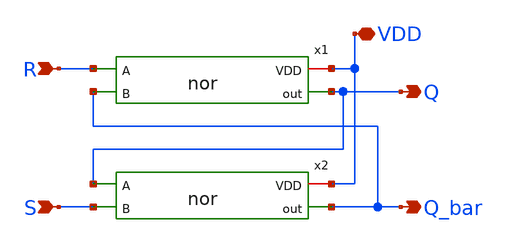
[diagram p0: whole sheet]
** sch_path: xschem/RS_latch.sch
**.subckt RS_latch VDD Q Q_bar R S
*.iopin VDD
*.opin Q
*.opin Q_bar
*.ipin R
*.ipin S
x1 VDD R Q_bar Q nor
x2 VDD Q S Q_bar nor
**.ends

* expanding   symbol:  nor.sym # of pins=4
** sym_path: xschem/nor.sym
** sch_path: xschem/nor.sch
.subckt nor VDD A B out
*.iopin VDD
*.ipin A
*.ipin B
*.opin out
XM1 out B GND GND sky130_fd_pr__nfet_01v8 L=0.18 W=0.42 nf=1 ad='int((nf+1)/2) * W/nf * 0.29' as='int((nf+2)/2) * W/nf * 0.29'
+ pd='2*int((nf+1)/2) * (W/nf + 0.29)' ps='2*int((nf+2)/2) * (W/nf + 0.29)' nrd='0.29 / W' nrs='0.29 / W'
+ sa=0 sb=0 sd=0 mult=1 m=1
XM2 out A GND GND sky130_fd_pr__nfet_01v8 L=0.18 W=0.42 nf=1 ad='int((nf+1)/2) * W/nf * 0.29' as='int((nf+2)/2) * W/nf * 0.29'
+ pd='2*int((nf+1)/2) * (W/nf + 0.29)' ps='2*int((nf+2)/2) * (W/nf + 0.29)' nrd='0.29 / W' nrs='0.29 / W'
+ sa=0 sb=0 sd=0 mult=1 m=1
XM3 out B net1 VDD sky130_fd_pr__pfet_01v8 L=0.18 W=0.84 nf=1 ad='int((nf+1)/2) * W/nf * 0.29' as='int((nf+2)/2) * W/nf * 0.29'
+ pd='2*int((nf+1)/2) * (W/nf + 0.29)' ps='2*int((nf+2)/2) * (W/nf + 0.29)' nrd='0.29 / W' nrs='0.29 / W'
+ sa=0 sb=0 sd=0 mult=1 m=1
XM4 net1 A VDD VDD sky130_fd_pr__pfet_01v8 L=0.18 W=0.84 nf=1 ad='int((nf+1)/2) * W/nf * 0.29' as='int((nf+2)/2) * W/nf * 0.29'
+ pd='2*int((nf+1)/2) * (W/nf + 0.29)' ps='2*int((nf+2)/2) * (W/nf + 0.29)' nrd='0.29 / W' nrs='0.29 / W'
+ sa=0 sb=0 sd=0 mult=1 m=1
.ends

.GLOBAL GND
.end
